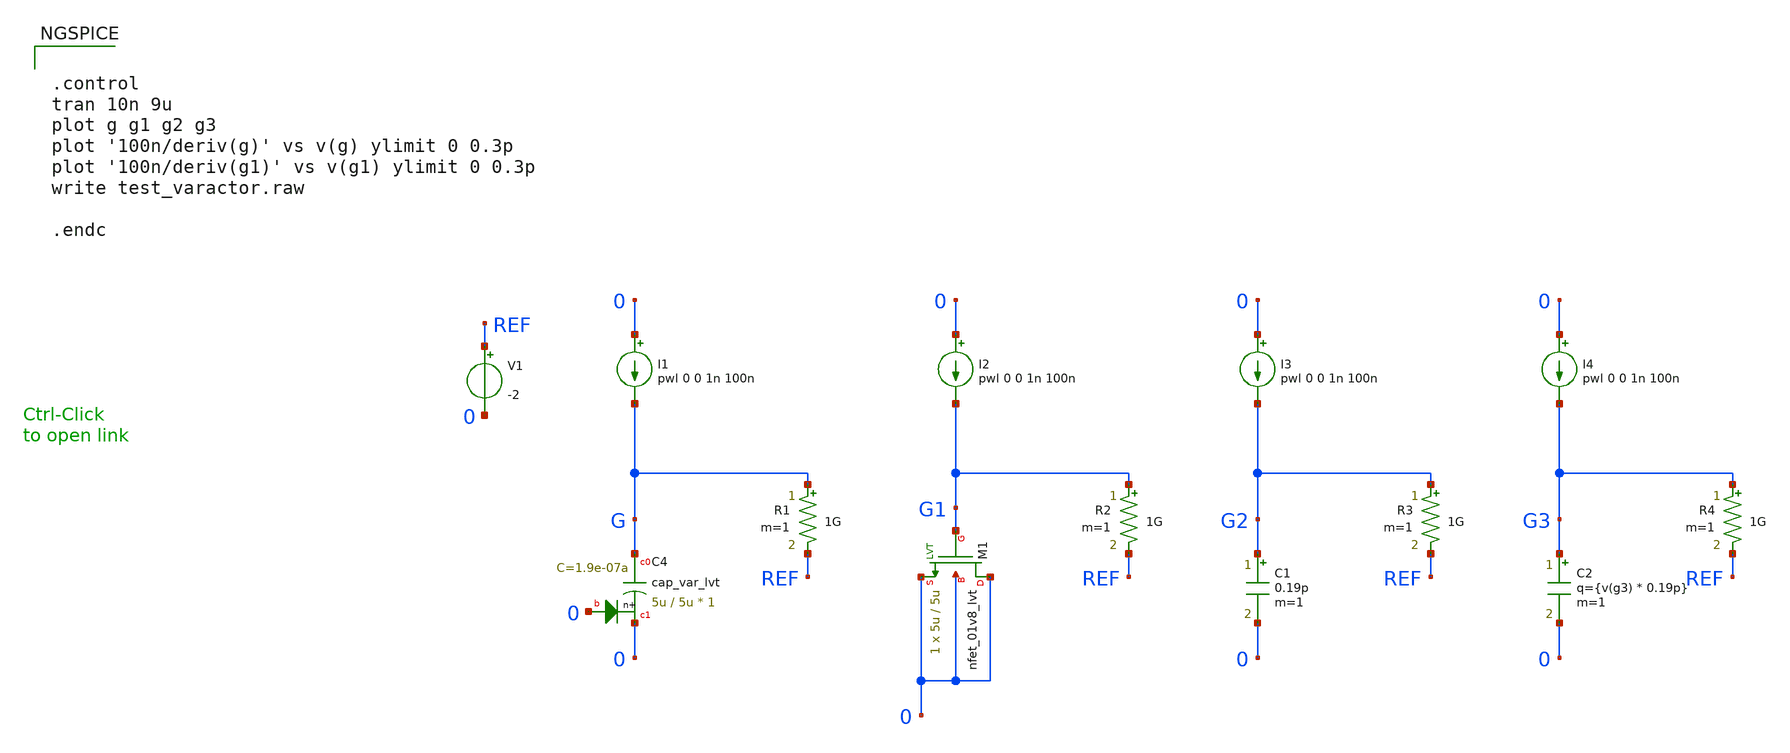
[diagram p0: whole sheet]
** sch_path: sky130_tests_X/test_varactor.sch
* Copyright 2020 Stefan Frederik Schippers
* Licensed under the Apache License, Version 2.0 (the "License");
* you may not use this file except in compliance with the License.
* You may obtain a copy of the License at
* https://www.apache.org/licenses/LICENSE-2.0
* Unless required by applicable law or agreed to in writing, software
* distributed under the License is distributed on an "AS IS" BASIS,
* WITHOUT WARRANTIES OR CONDITIONS OF ANY KIND, either express or implied.
* See the License for the specific language governing permissions and
* limitations under the License.
**.subckt test_varactor
I1 0 G pwl 0 0 1n 100n
R1 G REF 1G m=1
I2 0 G1 pwl 0 0 1n 100n
R2 G1 REF 1G m=1
I3 0 G2 pwl 0 0 1n 100n
R3 G2 REF 1G m=1
C1 G2 0 0.19p m=1
V1 REF 0 -2
XM1 0 G1 0 0 sky130_fd_pr__nfet_01v8_lvt w=5u l=5u ad='w * 0.29u' pd='2 * (w + 0.29u)' as='w * 0.29u'
+ ps='2 * (w + 0.29u)' nrd='0.29u / w' nrs='0.29u / w' sa=0 sb=0 sd=0 nf=1 mult=1 m=1
I4 0 G3 pwl 0 0 1n 100n
R4 G3 REF 1G m=1
C2 G3 0 q={v(g3) * 0.19p} m=1
XC4 G 0 0 sky130_fd_pr__cap_var_lvt W=5u L=5u VM=1 m=1
**** begin user architecture code


.control
tran 10n 9u
plot g g1 g2 g3
plot '100n/deriv(g)' vs v(g) ylimit 0 0.3p
plot '100n/deriv(g1)' vs v(g1) ylimit 0 0.3p
write test_varactor.raw

.endc



**** end user architecture code
**.ends
.end
